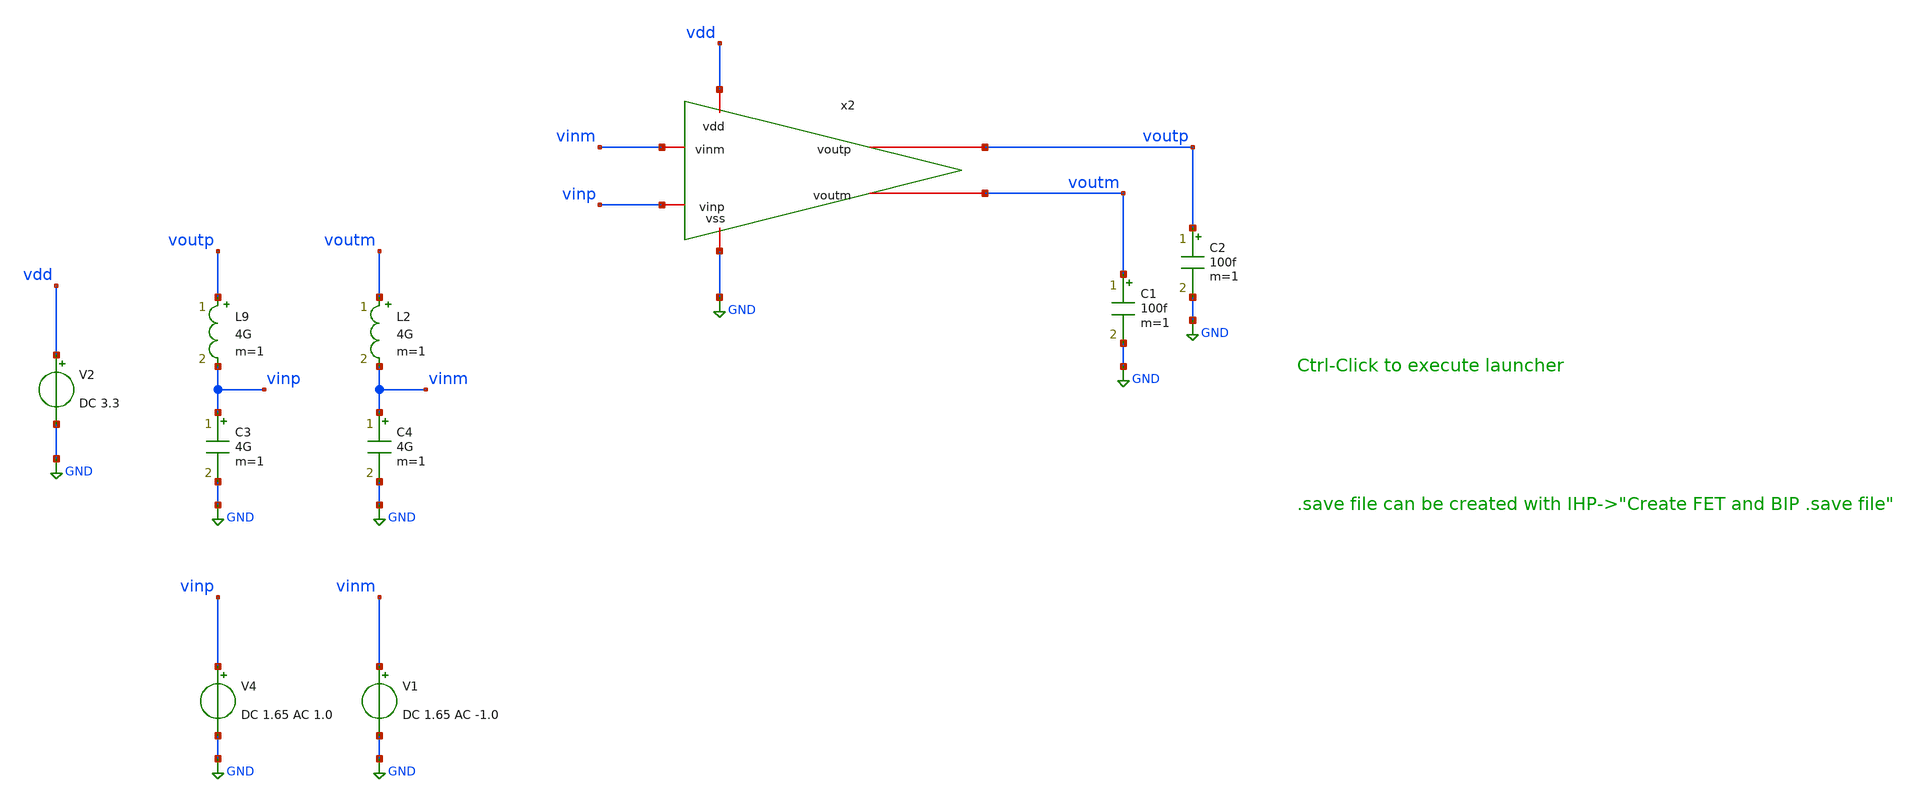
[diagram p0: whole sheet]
** sch_path: testbench/aux_amp_tb.sch
**.subckt aux_amp_tb
C2 voutp GND 100f m=1
V2 vdd GND DC 3.3
V4 vinp GND DC 1.65 AC 1.0
L9 voutp vinp 4G m=1
C3 vinp GND 4G m=1
x2 vdd vinm vinp voutp voutm GND aux_amp
C1 voutm GND 100f m=1
L2 voutm vinm 4G m=1
C4 vinm GND 4G m=1
V1 vinm GND DC 1.65 AC -1.0
**** begin user architecture code

.lib cornerMOShv.lib mos_tt
.lib $::SG13G2_MODELS/cornerCAP.lib cap_typ



.param temp=27
.include aux_amp_tb.save
.control
op
save all
write aux_amp_tb.raw
set appendwrite #writing into the same raw file
ac dec 100 1 100e6
save all

let Av = db(v(voutp))
let phase = 180/3.14*vp(voutp)
let CMRR = db((v(voutp)/v(vinp))/(v(voutp_cmrr)/v(vinp)))
let PSRR = db(v(voutp_psrr)/v(vdd_ac))

echo ---
meas ac gm_db find vdb(voutp) when vp(voutp)=0
meas ac pm_deg find phase when vdb(voutp)=0
meas ac _3db_f when phase=-45
meas ac _0db_f when vdb(voutp)=0
meas ac dc_gain find vdb(voutp) at=1
echo ---

write aux_amp_tb.raw
.endc


**** end user architecture code
**.ends

* expanding   symbol:  aux_amp.sym # of pins=6
** sym_path: schematic/aux_amp.sym
** sch_path: schematic/aux_amp.sch
.subckt aux_amp vdd vinm vinp voutp voutm vss
*.iopin vss
*.iopin voutm
*.iopin vinp
*.iopin vdd
*.iopin voutp
*.iopin vinm
XM2 net3 vinp net1 net1 sg13_hv_nmos w=0.3u l=0.45u ng=1 m=1 mm_ok=1
XM3 net4 cm_bias net1 net1 sg13_hv_nmos w=0.3u l=0.45u ng=1 m=1 mm_ok=1
XM4 net1 nbias vss vss sg13_hv_nmos w=0.3u l=0.45u ng=1 m=1 mm_ok=1
XM6 net3 cm_bias net2 net2 sg13_hv_nmos w=0.3u l=0.45u ng=1 m=1 mm_ok=1
XM7 net4 vinm net2 net2 sg13_hv_nmos w=0.3u l=0.45u ng=1 m=1 mm_ok=1
XM8 net2 nbias vss vss sg13_hv_nmos w=0.3u l=0.45u ng=1 m=1 mm_ok=1
XM9 voutm nbias vss vss sg13_hv_nmos w=0.3u l=0.45u ng=1 m=1 mm_ok=1
XM11 voutp nbias vss vss sg13_hv_nmos w=0.3u l=0.45u ng=1 m=1 mm_ok=1
V2 pbias_top vss 1.65
V3 pbias vss 1.65
V4 cm_bias vss 1.65
V1 nbias vss 1.65
XM1 voutm pbias net3 net3 sg13_hv_pmos w=0.3u l=0.4u ng=1 m=1 mm_ok=1
XM5 net3 pbias_top vdd vdd sg13_hv_pmos w=0.3u l=0.4u ng=1 m=1 mm_ok=1
XM10 net4 pbias_top vdd vdd sg13_hv_pmos w=0.3u l=0.4u ng=1 m=1 mm_ok=1
XM12 voutp pbias net4 net4 sg13_hv_pmos w=0.3u l=0.4u ng=1 m=1 mm_ok=1
.ends

.GLOBAL GND
.end
